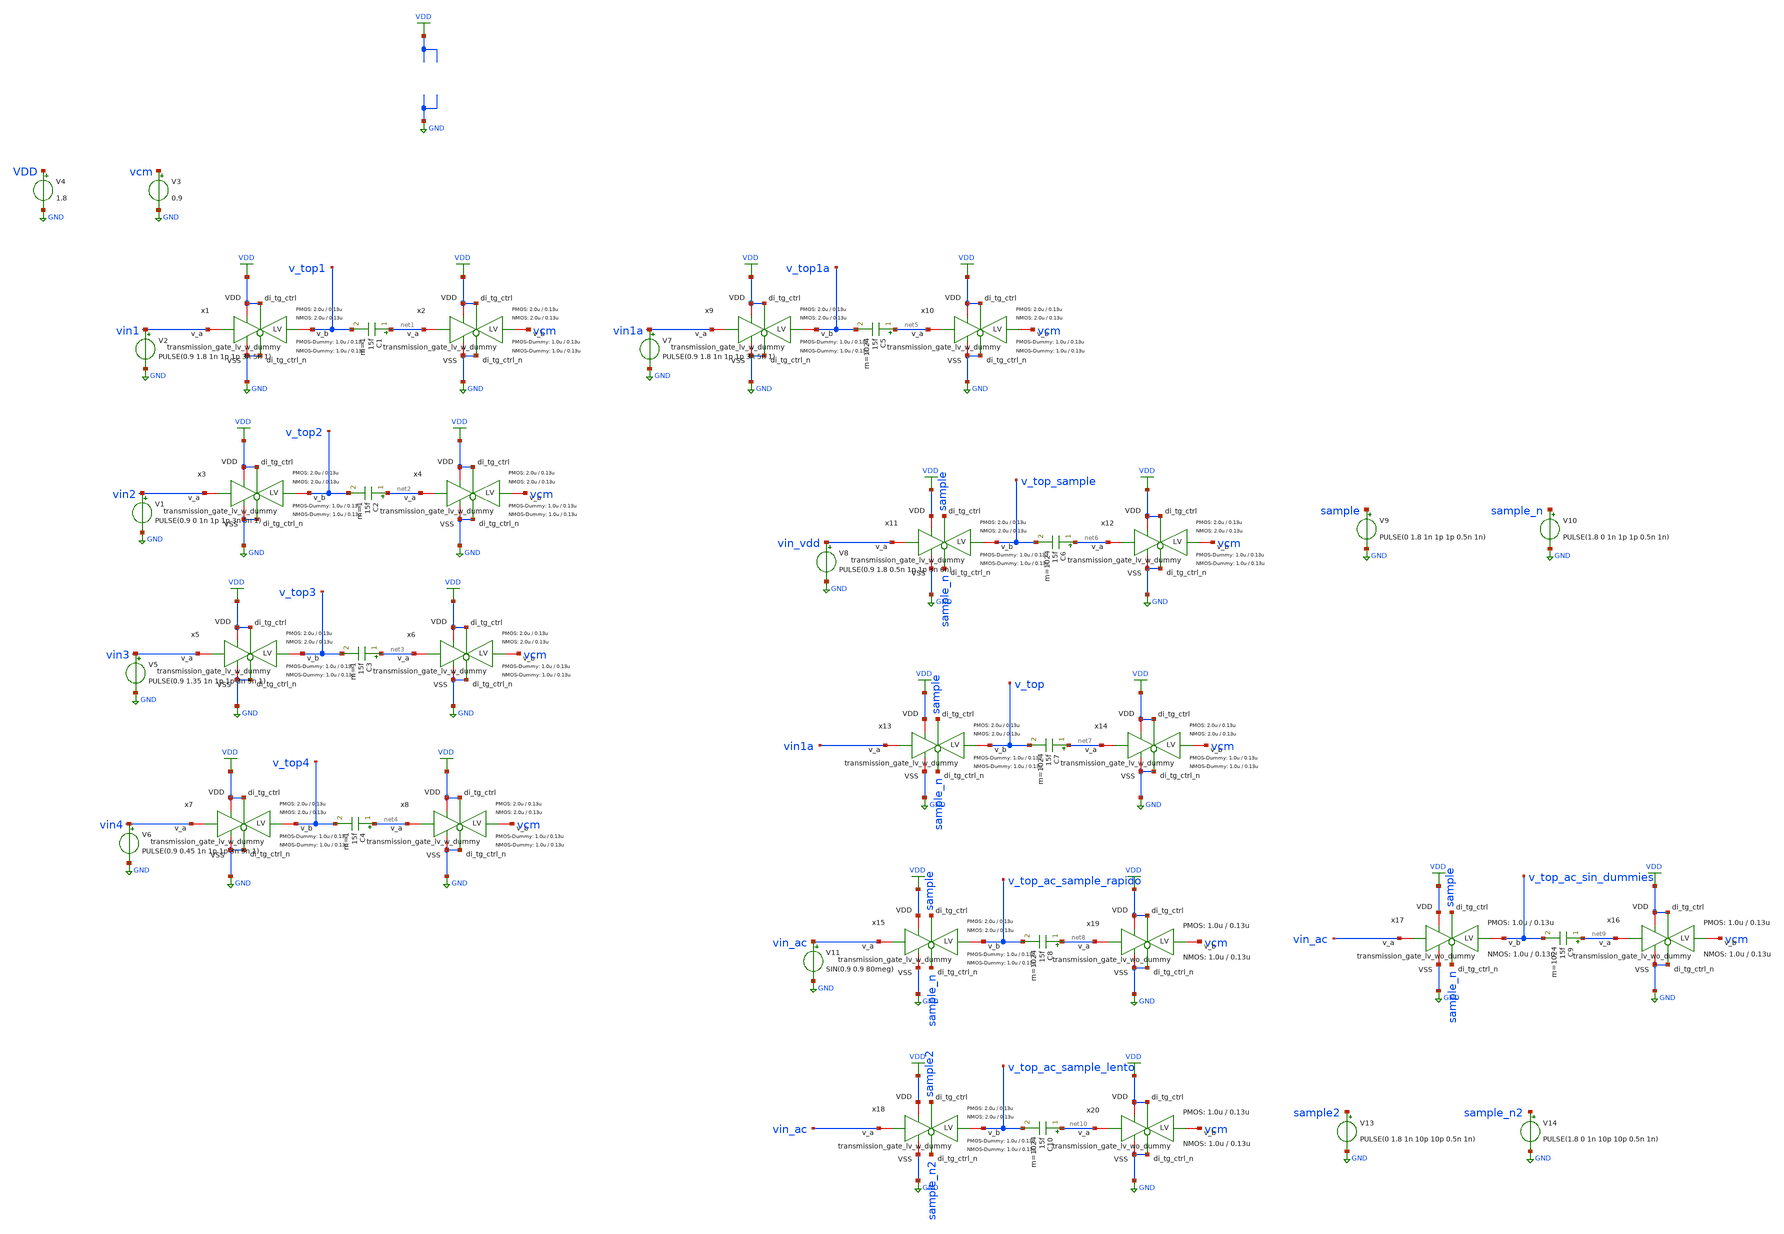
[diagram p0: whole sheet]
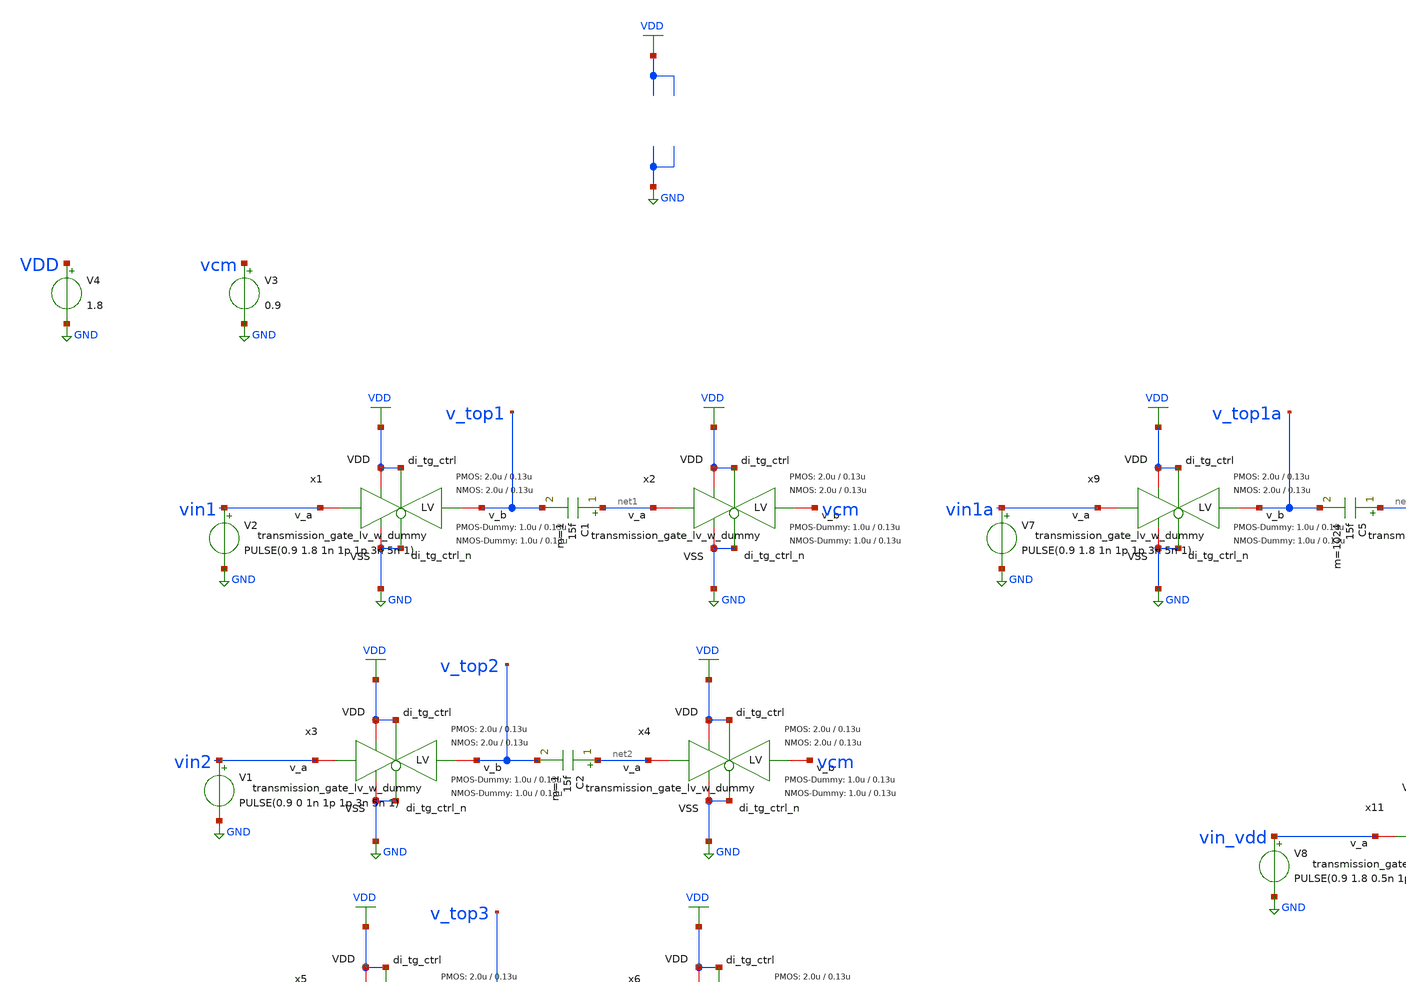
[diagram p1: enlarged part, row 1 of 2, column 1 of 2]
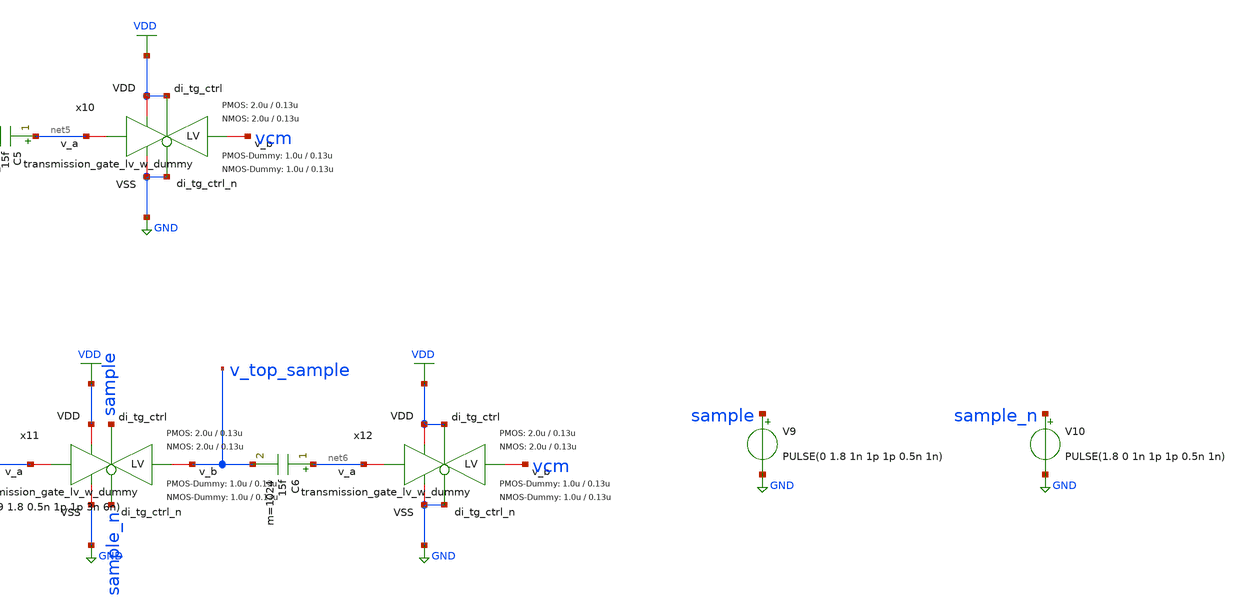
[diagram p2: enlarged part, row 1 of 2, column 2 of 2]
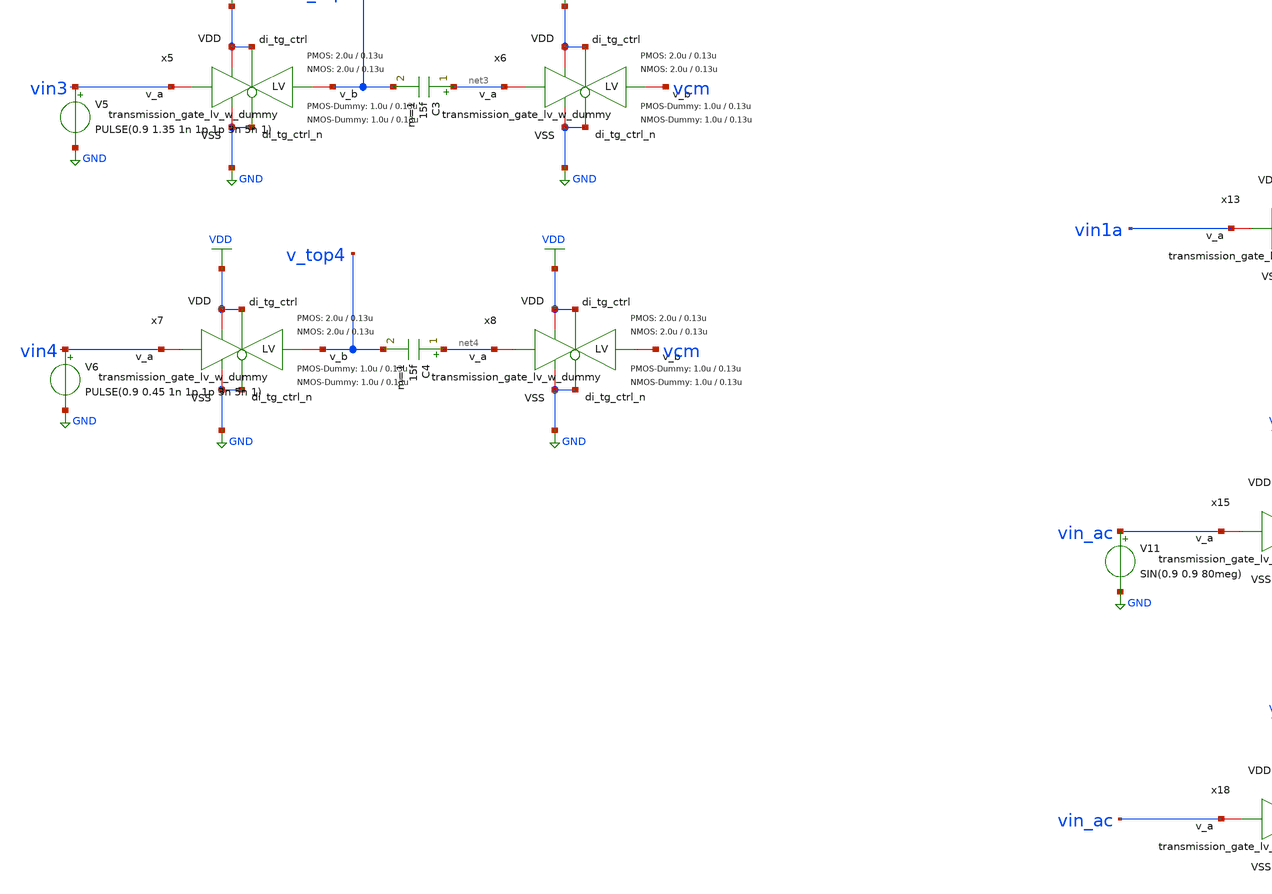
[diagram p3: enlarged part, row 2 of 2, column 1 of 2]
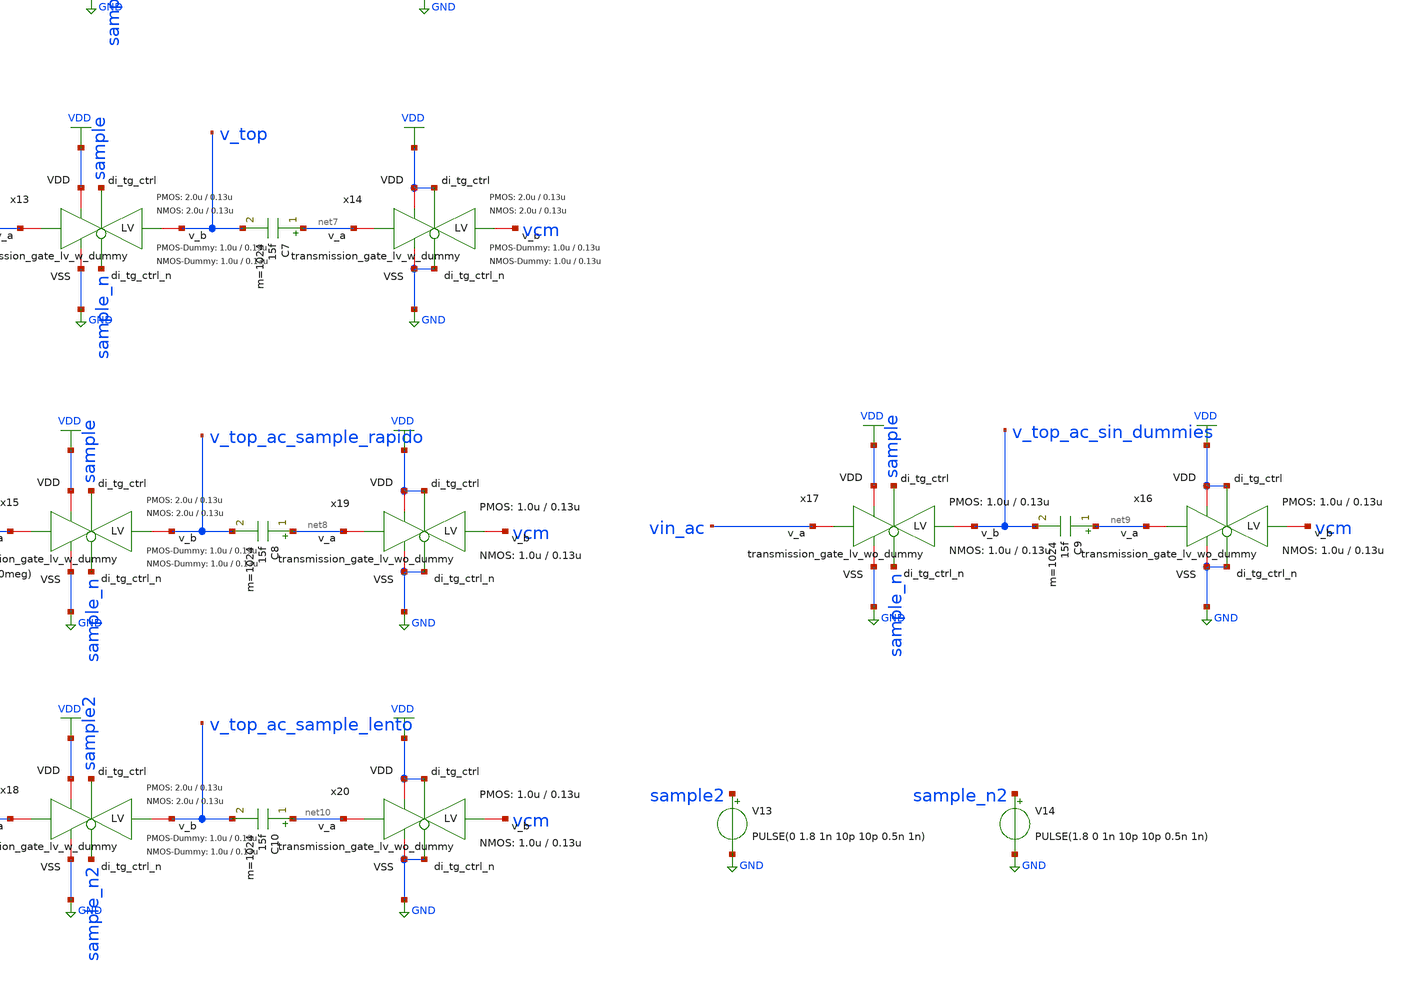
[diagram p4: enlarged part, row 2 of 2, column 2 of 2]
** sch_path: xschem/dac_icms_cell/testbenches/tb_top_tran_step.sch
**.subckt tb_top_tran_step
V2 vin1 GND PULSE(0.9 1.8 1n 1p 1p 3n 5n 1)
V3 vcm GND 0.9
V4 VDD GND 1.8
x1 VDD VDD GND v_top1 vin1 GND transmission_gate_lv_w_dummy W_P=2.0u L_P=0.13u W_N=2.0u L_N=0.13u
+ W_P_D=1.0u L_P_D=0.13u W_N_D=1.0u L_N_D=0.13u n=1
x2 VDD VDD GND vcm net1 GND transmission_gate_lv_w_dummy W_P=2.0u L_P=0.13u W_N=2.0u L_N=0.13u
+ W_P_D=1.0u L_P_D=0.13u W_N_D=1.0u L_N_D=0.13u n=1
C1 net1 v_top1 15f m=1
V1 vin2 GND PULSE(0.9 0 1n 1p 1p 3n 5n 1)
x3 VDD VDD GND v_top2 vin2 GND transmission_gate_lv_w_dummy W_P=2.0u L_P=0.13u W_N=2.0u L_N=0.13u
+ W_P_D=1.0u L_P_D=0.13u W_N_D=1.0u L_N_D=0.13u n=1
x4 VDD VDD GND vcm net2 GND transmission_gate_lv_w_dummy W_P=2.0u L_P=0.13u W_N=2.0u L_N=0.13u
+ W_P_D=1.0u L_P_D=0.13u W_N_D=1.0u L_N_D=0.13u n=1
C2 net2 v_top2 15f m=1
V5 vin3 GND PULSE(0.9 1.35 1n 1p 1p 3n 5n 1)
x5 VDD VDD GND v_top3 vin3 GND transmission_gate_lv_w_dummy W_P=2.0u L_P=0.13u W_N=2.0u L_N=0.13u
+ W_P_D=1.0u L_P_D=0.13u W_N_D=1.0u L_N_D=0.13u n=1
x6 VDD VDD GND vcm net3 GND transmission_gate_lv_w_dummy W_P=2.0u L_P=0.13u W_N=2.0u L_N=0.13u
+ W_P_D=1.0u L_P_D=0.13u W_N_D=1.0u L_N_D=0.13u n=1
C3 net3 v_top3 15f m=1
V6 vin4 GND PULSE(0.9 0.45 1n 1p 1p 3n 5n 1)
x7 VDD VDD GND v_top4 vin4 GND transmission_gate_lv_w_dummy W_P=2.0u L_P=0.13u W_N=2.0u L_N=0.13u
+ W_P_D=1.0u L_P_D=0.13u W_N_D=1.0u L_N_D=0.13u n=1
x8 VDD VDD GND vcm net4 GND transmission_gate_lv_w_dummy W_P=2.0u L_P=0.13u W_N=2.0u L_N=0.13u
+ W_P_D=1.0u L_P_D=0.13u W_N_D=1.0u L_N_D=0.13u n=1
C4 net4 v_top4 15f m=1
V7 vin1a GND PULSE(0.9 1.8 1n 1p 1p 3n 5n 1)
x9 VDD VDD GND v_top1a vin1a GND transmission_gate_lv_w_dummy W_P=2.0u L_P=0.13u W_N=2.0u L_N=0.13u
+ W_P_D=1.0u L_P_D=0.13u W_N_D=1.0u L_N_D=0.13u n=1024
x10 VDD VDD GND vcm net5 GND transmission_gate_lv_w_dummy W_P=2.0u L_P=0.13u W_N=2.0u L_N=0.13u
+ W_P_D=1.0u L_P_D=0.13u W_N_D=1.0u L_N_D=0.13u n=1024
C5 net5 v_top1a 15f m=1024
x11 VDD sample GND v_top_sample vin_vdd sample_n transmission_gate_lv_w_dummy W_P=2.0u L_P=0.13u
+ W_N=2.0u L_N=0.13u W_P_D=1.0u L_P_D=0.13u W_N_D=1.0u L_N_D=0.13u n=1024
x12 VDD VDD GND vcm net6 GND transmission_gate_lv_w_dummy W_P=2.0u L_P=0.13u W_N=2.0u L_N=0.13u
+ W_P_D=1.0u L_P_D=0.13u W_N_D=1.0u L_N_D=0.13u n=1024
C6 net6 v_top_sample 15f m=1024
V9 sample GND PULSE(0 1.8 1n 1p 1p 0.5n 1n)
V10 sample_n GND PULSE(1.8 0 1n 1p 1p 0.5n 1n)
x13 VDD sample GND v_top vin1a sample_n transmission_gate_lv_w_dummy W_P=2.0u L_P=0.13u W_N=2.0u
+ L_N=0.13u W_P_D=1.0u L_P_D=0.13u W_N_D=1.0u L_N_D=0.13u n=1024
x14 VDD VDD GND vcm net7 GND transmission_gate_lv_w_dummy W_P=2.0u L_P=0.13u W_N=2.0u L_N=0.13u
+ W_P_D=1.0u L_P_D=0.13u W_N_D=1.0u L_N_D=0.13u n=1024
C7 net7 v_top 15f m=1024
V8 vin_vdd GND PULSE(0.9 1.8 0.5n 1p 1p 3n 6n)
x15 VDD sample GND v_top_ac_sample_rapido vin_ac sample_n transmission_gate_lv_w_dummy W_P=2.0u
+ L_P=0.13u W_N=2.0u L_N=0.13u W_P_D=1.0u L_P_D=0.13u W_N_D=1.0u L_N_D=0.13u n=1024
C8 net8 v_top_ac_sample_rapido 15f m=1024
V11 vin_ac GND SIN(0.9 0.9 80meg)
C9 net9 v_top_ac_sin_dummies 15f m=1024
x19 VDD VDD GND vcm net8 GND transmission_gate_lv_wo_dummy W_P=1.0u L_P=0.13u W_N=1.0u L_N=0.13u
+ W_P_D=1.0u L_P_D=0.13u W_N_D=1.0u L_N_D=0.13u n=1024
x16 VDD VDD GND vcm net9 GND transmission_gate_lv_wo_dummy W_P=1.0u L_P=0.13u W_N=1.0u L_N=0.13u
+ W_P_D=1.0u L_P_D=0.13u W_N_D=1.0u L_N_D=0.13u n=1024
x17 VDD sample GND v_top_ac_sin_dummies vin_ac sample_n transmission_gate_lv_wo_dummy W_P=1.0u
+ L_P=0.13u W_N=1.0u L_N=0.13u W_P_D=1.0u L_P_D=0.13u W_N_D=1.0u L_N_D=0.13u n=1024
x18 VDD sample2 GND v_top_ac_sample_lento vin_ac sample_n2 transmission_gate_lv_w_dummy W_P=2.0u
+ L_P=0.13u W_N=2.0u L_N=0.13u W_P_D=1.0u L_P_D=0.13u W_N_D=1.0u L_N_D=0.13u n=1024
C10 net10 v_top_ac_sample_lento 15f m=1024
x20 VDD VDD GND vcm net10 GND transmission_gate_lv_wo_dummy W_P=1.0u L_P=0.13u W_N=1.0u L_N=0.13u
+ W_P_D=1.0u L_P_D=0.13u W_N_D=1.0u L_N_D=0.13u n=1024
V13 sample2 GND PULSE(0 1.8 1n 10p 10p 0.5n 1n)
V14 sample_n2 GND PULSE(1.8 0 1n 10p 10p 0.5n 1n)
**** begin user architecture code


.param temp=27
.param period = 2n
.param wp = 1.5u
.param wn = 0.5u
.param rise_t = period*0.01
.param fall_t = period*0.01
.param delay_n = 0
.param delay_s = 0
.param delay_2 = period*0.2
.param delay_1 = period*0
.options savecurrents klu method=gear reltol=1e-2 abstol=1e-15 gmin=1e-10

.control
set hcopydevtype = svg
set color0 = white
set color1 = black

tran .1p 4n



plot vin1 vin2 vin3 vin4 v_top1 v_top2 v_top3 v_top4
plot vin1a v_top1a
plot vin1a+2 sample+2 v_top v_top_sample
plot v_top v_top1 v_top_sample
plo vin_ac v_top_ac v_top_ac_sin_dummies

hardcopy ./../../img/rise_top.svg vin1 vin2 vin3 vin4 v_top1 v_top2 v_top3 v_top4 xlimit 1n 1.1n title
+ 'Pulso de subida'
hardcopy ./../../img/fall_top.svg vin1 vin2 vin3 vin4 v_top1 v_top2 v_top3 v_top4 xlimit 4n 4.1n title
+ 'Pulso de bajada'
hardcopy ./../../img/rise_topa.svg vin1  v_top1 v_top1a xlimit 4n 4.1n title 'Pulso de subida de 1024 circuitos en paralelo'
hardcopy ./../../img/delays_sah.svg v_top v_top1 v_top_sample xlimit 1n 1.1n title 'Comparativa Retardos'
hardcopy ./../../img/respuesta_c.svg vin_ac v_top_ac_sample_rapido  title 'Ejemplo de sample a 80MHz'
hardcopy ./../../img/sample_rapido_vs_lento_dummies.svg vin_ac  v_top_ac_sample_rapido v_top_ac_sample_lento
+  v_top_ac_sin_dummies title 'Efecto del tiempo de bajada de sample en la inyeccion de carga'
hardcopy ./../../img/sample_rapido_vs_lento_dummies_zoom.svg vin_ac  v_top_ac_sample_rapido v_top_ac_sample_lento
+  v_top_ac_sin_dummies ylimit 1.7 1.9 xlimit 3.4n 3.8n title 'Efecto del tiempo de bajada de sample en la inyeccion de carga'
.endc




** IHP models
.lib cornerMOSlv.lib mos_tt
.lib cornerMOShv.lib mos_tt
.lib cornerHBT.lib hbt_typ
.lib cornerRES.lib res_typ
.include /foss/pdks/ihp-sg13g2/libs.ref/sg13g2_stdcell/spice/sg13g2_stdcell.spice


**** end user architecture code
**.ends

* expanding   symbol:  transmission_gate/transmission_gate_lv_w_dummy.sym # of pins=6
** sym_path: xschem/transmission_gate/transmission_gate_lv_w_dummy.sym
** sch_path: xschem/transmission_gate/transmission_gate_lv_w_dummy.sch
.subckt transmission_gate_lv_w_dummy VDD di_tg_ctrl VSS v_b v_a di_tg_ctrl_n  W_P=2.0u L_P=0.13u
+ W_N=2.0u L_N=0.13u W_P_D=1.0u L_P_D=0.13u W_N_D=1.0u L_N_D=0.13u n=1
*.iopin v_a
*.iopin v_b
*.iopin VDD
*.iopin VSS
*.ipin di_tg_ctrl
*.ipin di_tg_ctrl_n
XM1 v_a di_tg_ctrl v_b VSS sg13_lv_nmos w={2*W_N} l=L_N ng=1 m={n} mm_ok=1
XM2 v_a di_tg_ctrl_n v_b VDD sg13_lv_pmos w={2*W_P} l=L_P ng=1 m={n} mm_ok=1
XMdummy2 v_b di_tg_ctrl v_b VDD sg13_lv_pmos w=W_P l=L_P ng=1 m=n mm_ok=1
XMdummy1 v_b di_tg_ctrl_n v_b VSS sg13_lv_nmos w=W_N l=L_N ng=1 m=n mm_ok=1
.ends


* expanding   symbol:  transmission_gate/transmission_gate_lv_wo_dummy.sym # of pins=6
** sym_path: xschem/transmission_gate/transmission_gate_lv_wo_dummy.sym
** sch_path: xschem/transmission_gate/transmission_gate_lv_wo_dummy.sch
.subckt transmission_gate_lv_wo_dummy VDD di_tg_ctrl VSS v_b v_a di_tg_ctrl_n  W_P=2.0u L_P=0.13u
+ W_N=2.0u L_N=0.13u W_P_D=1.0u L_P_D=0.13u W_N_D=1.0u L_N_D=0.13u n=1
*.iopin v_a
*.iopin v_b
*.iopin VDD
*.iopin VSS
*.ipin di_tg_ctrl
*.ipin di_tg_ctrl_n
XM1 v_a di_tg_ctrl v_b VSS sg13_lv_nmos w=W_N l=L_N ng=1 m=n mm_ok=1
XM2 v_a di_tg_ctrl_n v_b VDD sg13_lv_pmos w=W_P l=L_P ng=1 m=n mm_ok=1
.ends

.GLOBAL GND
.GLOBAL VDD
.end
